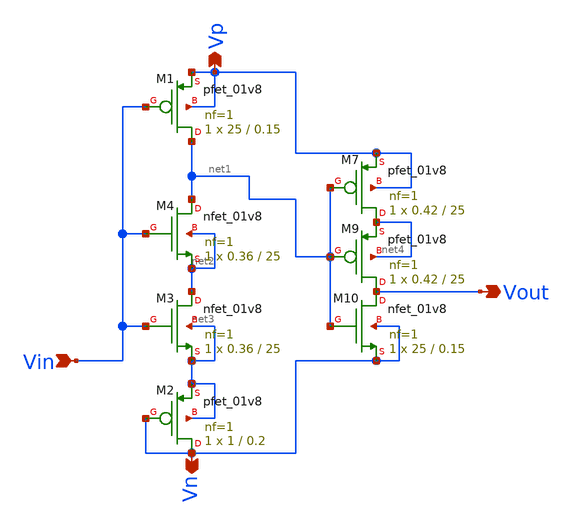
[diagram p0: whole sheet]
** sch_path: xschem/Vth_sch/Symbol/th15.sch
**.subckt th15 Vin Vout Vp Vn
*.ipin Vin
*.opin Vout
*.opin Vp
*.opin Vn
XM1 net1 Vin Vp Vp sky130_fd_pr__pfet_01v8 L=0.15 W=25 nf=1 ad='int((nf+1)/2) * W/nf * 0.29' as='int((nf+2)/2) * W/nf * 0.29'
+ pd='2*int((nf+1)/2) * (W/nf + 0.29)' ps='2*int((nf+2)/2) * (W/nf + 0.29)' nrd='0.29 / W' nrs='0.29 / W'
+ sa=0 sb=0 sd=0 mult=1 m=1
XM3 net2 Vin net3 net3 sky130_fd_pr__nfet_01v8 L=25 W=0.36 nf=1 ad='int((nf+1)/2) * W/nf * 0.29' as='int((nf+2)/2) * W/nf * 0.29'
+ pd='2*int((nf+1)/2) * (W/nf + 0.29)' ps='2*int((nf+2)/2) * (W/nf + 0.29)' nrd='0.29 / W' nrs='0.29 / W'
+ sa=0 sb=0 sd=0 mult=1 m=1
XM4 net1 Vin net2 net2 sky130_fd_pr__nfet_01v8 L=25 W=0.36 nf=1 ad='int((nf+1)/2) * W/nf * 0.29' as='int((nf+2)/2) * W/nf * 0.29'
+ pd='2*int((nf+1)/2) * (W/nf + 0.29)' ps='2*int((nf+2)/2) * (W/nf + 0.29)' nrd='0.29 / W' nrs='0.29 / W'
+ sa=0 sb=0 sd=0 mult=1 m=1
XM2 Vn Vn net3 net3 sky130_fd_pr__pfet_01v8 L=0.2 W=1 nf=1 ad='int((nf+1)/2) * W/nf * 0.29' as='int((nf+2)/2) * W/nf * 0.29'
+ pd='2*int((nf+1)/2) * (W/nf + 0.29)' ps='2*int((nf+2)/2) * (W/nf + 0.29)' nrd='0.29 / W' nrs='0.29 / W'
+ sa=0 sb=0 sd=0 mult=1 m=1
XM7 net4 net1 Vp Vp sky130_fd_pr__pfet_01v8 L=25 W=0.42 nf=1 ad='int((nf+1)/2) * W/nf * 0.29' as='int((nf+2)/2) * W/nf * 0.29'
+ pd='2*int((nf+1)/2) * (W/nf + 0.29)' ps='2*int((nf+2)/2) * (W/nf + 0.29)' nrd='0.29 / W' nrs='0.29 / W'
+ sa=0 sb=0 sd=0 mult=1 m=1
XM9 Vout net1 net4 net4 sky130_fd_pr__pfet_01v8 L=25 W=0.42 nf=1 ad='int((nf+1)/2) * W/nf * 0.29' as='int((nf+2)/2) * W/nf * 0.29'
+ pd='2*int((nf+1)/2) * (W/nf + 0.29)' ps='2*int((nf+2)/2) * (W/nf + 0.29)' nrd='0.29 / W' nrs='0.29 / W'
+ sa=0 sb=0 sd=0 mult=1 m=1
XM10 Vout net1 Vn Vn sky130_fd_pr__nfet_01v8 L=0.15 W=25 nf=1 ad='int((nf+1)/2) * W/nf * 0.29' as='int((nf+2)/2) * W/nf * 0.29'
+ pd='2*int((nf+1)/2) * (W/nf + 0.29)' ps='2*int((nf+2)/2) * (W/nf + 0.29)' nrd='0.29 / W' nrs='0.29 / W'
+ sa=0 sb=0 sd=0 mult=1 m=1
**.ends
.end
